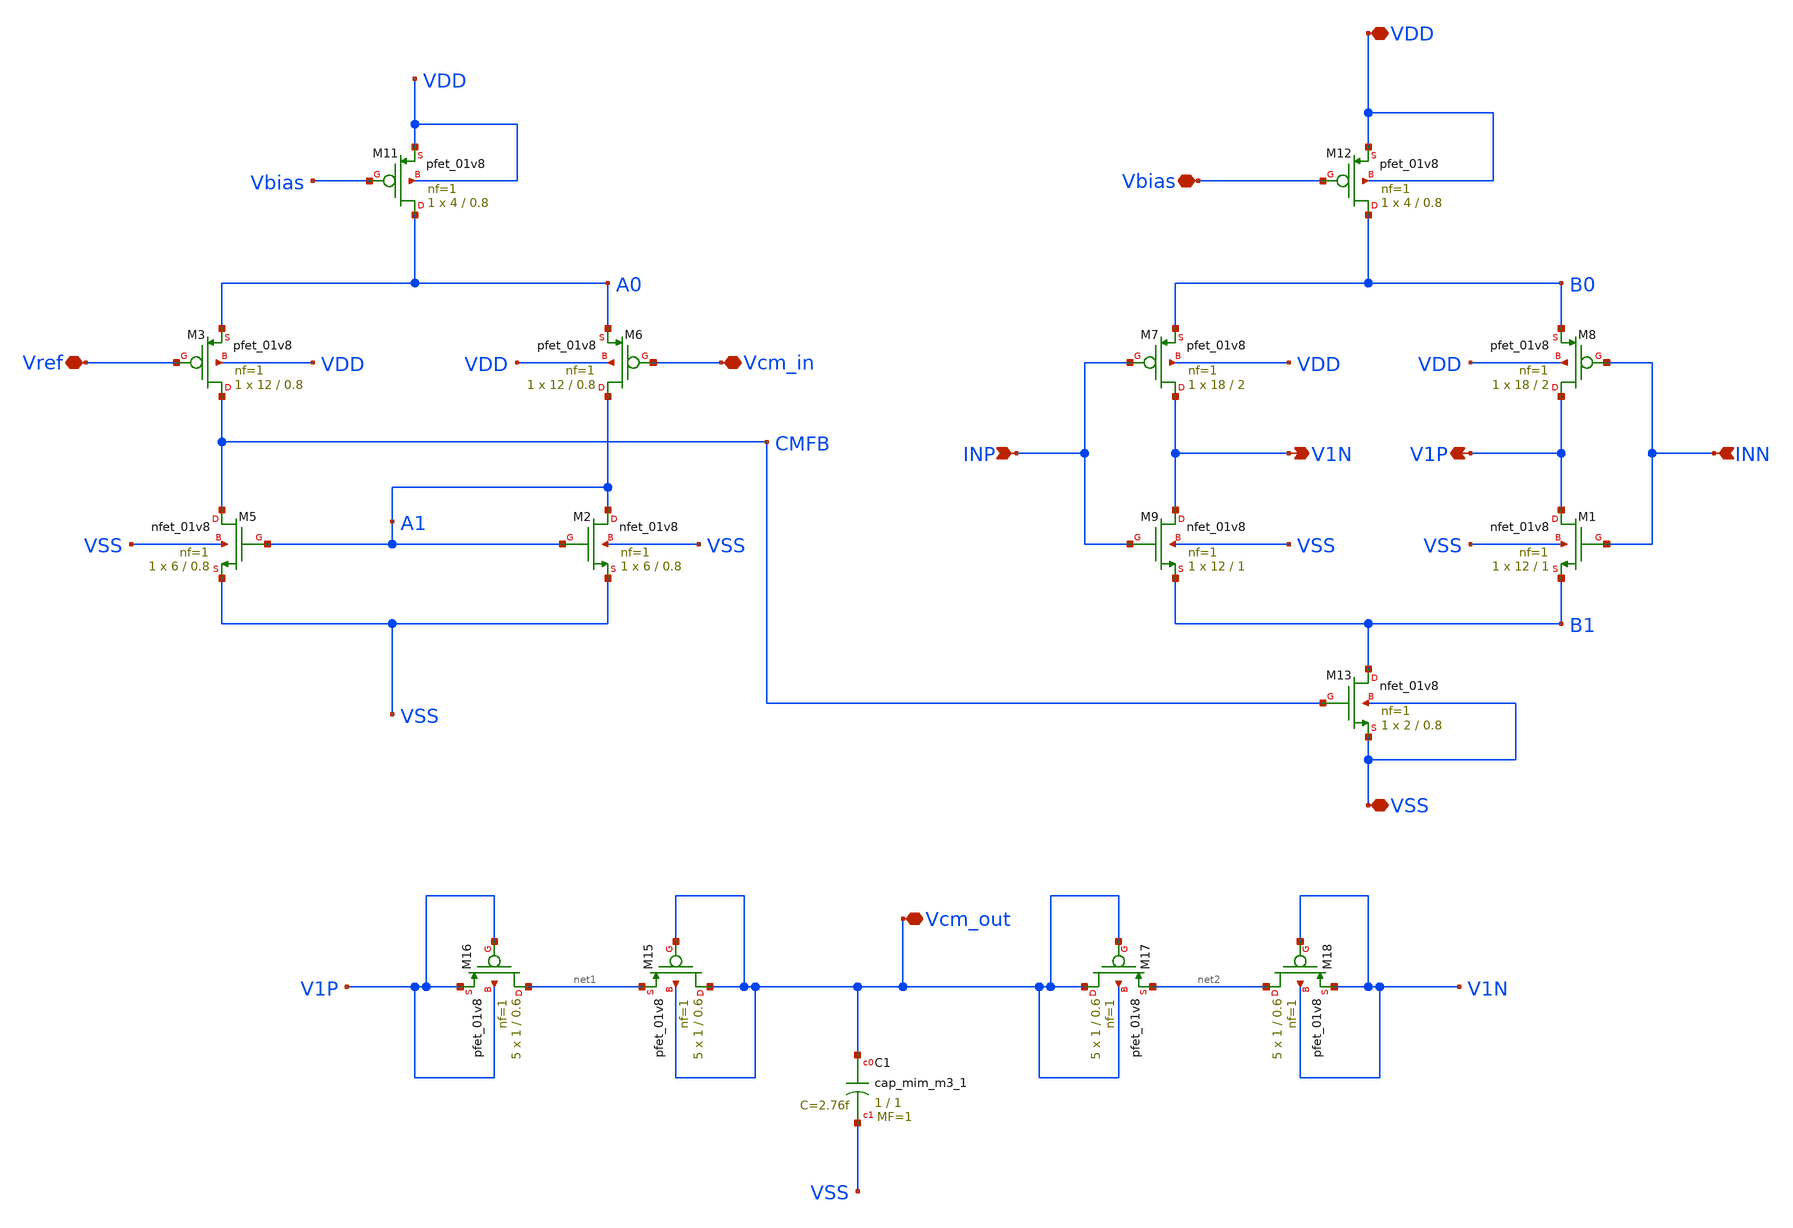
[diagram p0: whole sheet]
** sch_path: opamp_lna/low_noise_amp.sch
**.subckt low_noise_amp VDD VSS Vbias INP INN Vref Vcm_in Vcm_out V1N V1P
*.iopin VDD
*.iopin VSS
*.iopin Vbias
*.ipin INP
*.ipin INN
*.iopin Vref
*.iopin Vcm_in
*.iopin Vcm_out
*.opin V1N
*.opin V1P
XM3 CMFB Vref A0 VDD sky130_fd_pr__pfet_01v8 L=0.8 W=12 nf=1 ad='int((nf+1)/2) * W/nf * 0.29' as='int((nf+2)/2) * W/nf * 0.29'
+ pd='2*int((nf+1)/2) * (W/nf + 0.29)' ps='2*int((nf+2)/2) * (W/nf + 0.29)' nrd='0.29 / W' nrs='0.29 / W'
+ sa=0 sb=0 sd=0 mult=1 m=1
XM11 A0 Vbias VDD VDD sky130_fd_pr__pfet_01v8 L=0.8 W=4 nf=1 ad='int((nf+1)/2) * W/nf * 0.29' as='int((nf+2)/2) * W/nf * 0.29'
+ pd='2*int((nf+1)/2) * (W/nf + 0.29)' ps='2*int((nf+2)/2) * (W/nf + 0.29)' nrd='0.29 / W' nrs='0.29 / W'
+ sa=0 sb=0 sd=0 mult=1 m=1
XM7 V1N INP B0 VDD sky130_fd_pr__pfet_01v8 L=2 W=18 nf=1 ad='int((nf+1)/2) * W/nf * 0.29' as='int((nf+2)/2) * W/nf * 0.29'
+ pd='2*int((nf+1)/2) * (W/nf + 0.29)' ps='2*int((nf+2)/2) * (W/nf + 0.29)' nrd='0.29 / W' nrs='0.29 / W'
+ sa=0 sb=0 sd=0 mult=1 m=1
XM8 V1P INN B0 VDD sky130_fd_pr__pfet_01v8 L=2 W=18 nf=1 ad='int((nf+1)/2) * W/nf * 0.29' as='int((nf+2)/2) * W/nf * 0.29'
+ pd='2*int((nf+1)/2) * (W/nf + 0.29)' ps='2*int((nf+2)/2) * (W/nf + 0.29)' nrd='0.29 / W' nrs='0.29 / W'
+ sa=0 sb=0 sd=0 mult=1 m=1
XM9 V1N INP B1 VSS sky130_fd_pr__nfet_01v8 L=1 W=12 nf=1 ad='int((nf+1)/2) * W/nf * 0.29' as='int((nf+2)/2) * W/nf * 0.29'
+ pd='2*int((nf+1)/2) * (W/nf + 0.29)' ps='2*int((nf+2)/2) * (W/nf + 0.29)' nrd='0.29 / W' nrs='0.29 / W'
+ sa=0 sb=0 sd=0 mult=1 m=1
XM12 B0 Vbias VDD VDD sky130_fd_pr__pfet_01v8 L=0.8 W=4 nf=1 ad='int((nf+1)/2) * W/nf * 0.29' as='int((nf+2)/2) * W/nf * 0.29'
+ pd='2*int((nf+1)/2) * (W/nf + 0.29)' ps='2*int((nf+2)/2) * (W/nf + 0.29)' nrd='0.29 / W' nrs='0.29 / W'
+ sa=0 sb=0 sd=0 mult=1 m=1
XM13 B1 CMFB VSS VSS sky130_fd_pr__nfet_01v8 L=0.8 W=2 nf=1 ad='int((nf+1)/2) * W/nf * 0.29' as='int((nf+2)/2) * W/nf * 0.29'
+ pd='2*int((nf+1)/2) * (W/nf + 0.29)' ps='2*int((nf+2)/2) * (W/nf + 0.29)' nrd='0.29 / W' nrs='0.29 / W'
+ sa=0 sb=0 sd=0 mult=1 m=1
XM15 Vcm_out Vcm_out net1 Vcm_out sky130_fd_pr__pfet_01v8 L=0.6 W=1 nf=1 ad='int((nf+1)/2) * W/nf * 0.29'
+ as='int((nf+2)/2) * W/nf * 0.29' pd='2*int((nf+1)/2) * (W/nf + 0.29)' ps='2*int((nf+2)/2) * (W/nf + 0.29)'
+ nrd='0.29 / W' nrs='0.29 / W' sa=0 sb=0 sd=0 mult=5 m=5
XM16 net1 V1P V1P V1P sky130_fd_pr__pfet_01v8 L=0.6 W=1 nf=1 ad='int((nf+1)/2) * W/nf * 0.29' as='int((nf+2)/2) * W/nf * 0.29'
+ pd='2*int((nf+1)/2) * (W/nf + 0.29)' ps='2*int((nf+2)/2) * (W/nf + 0.29)' nrd='0.29 / W' nrs='0.29 / W'
+ sa=0 sb=0 sd=0 mult=5 m=5
XM17 Vcm_out Vcm_out net2 Vcm_out sky130_fd_pr__pfet_01v8 L=0.6 W=1 nf=1 ad='int((nf+1)/2) * W/nf * 0.29'
+ as='int((nf+2)/2) * W/nf * 0.29' pd='2*int((nf+1)/2) * (W/nf + 0.29)' ps='2*int((nf+2)/2) * (W/nf + 0.29)'
+ nrd='0.29 / W' nrs='0.29 / W' sa=0 sb=0 sd=0 mult=5 m=5
XM18 net2 V1N V1N V1N sky130_fd_pr__pfet_01v8 L=0.6 W=1 nf=1 ad='int((nf+1)/2) * W/nf * 0.29' as='int((nf+2)/2) * W/nf * 0.29'
+ pd='2*int((nf+1)/2) * (W/nf + 0.29)' ps='2*int((nf+2)/2) * (W/nf + 0.29)' nrd='0.29 / W' nrs='0.29 / W'
+ sa=0 sb=0 sd=0 mult=5 m=5
XC1 Vcm_out VSS sky130_fd_pr__cap_mim_m3_1 W=1 L=1 MF=1 m=1
XM1 V1P INN B1 VSS sky130_fd_pr__nfet_01v8 L=1 W=12 nf=1 ad='int((nf+1)/2) * W/nf * 0.29' as='int((nf+2)/2) * W/nf * 0.29'
+ pd='2*int((nf+1)/2) * (W/nf + 0.29)' ps='2*int((nf+2)/2) * (W/nf + 0.29)' nrd='0.29 / W' nrs='0.29 / W'
+ sa=0 sb=0 sd=0 mult=1 m=1
XM2 A1 A1 VSS VSS sky130_fd_pr__nfet_01v8 L=0.8 W=6 nf=1 ad='int((nf+1)/2) * W/nf * 0.29' as='int((nf+2)/2) * W/nf * 0.29'
+ pd='2*int((nf+1)/2) * (W/nf + 0.29)' ps='2*int((nf+2)/2) * (W/nf + 0.29)' nrd='0.29 / W' nrs='0.29 / W'
+ sa=0 sb=0 sd=0 mult=1 m=1
XM5 CMFB A1 VSS VSS sky130_fd_pr__nfet_01v8 L=0.8 W=6 nf=1 ad='int((nf+1)/2) * W/nf * 0.29' as='int((nf+2)/2) * W/nf * 0.29'
+ pd='2*int((nf+1)/2) * (W/nf + 0.29)' ps='2*int((nf+2)/2) * (W/nf + 0.29)' nrd='0.29 / W' nrs='0.29 / W'
+ sa=0 sb=0 sd=0 mult=1 m=1
XM6 A1 Vcm_in A0 VDD sky130_fd_pr__pfet_01v8 L=0.8 W=12 nf=1 ad='int((nf+1)/2) * W/nf * 0.29' as='int((nf+2)/2) * W/nf * 0.29'
+ pd='2*int((nf+1)/2) * (W/nf + 0.29)' ps='2*int((nf+2)/2) * (W/nf + 0.29)' nrd='0.29 / W' nrs='0.29 / W'
+ sa=0 sb=0 sd=0 mult=1 m=1
**.ends
.end
